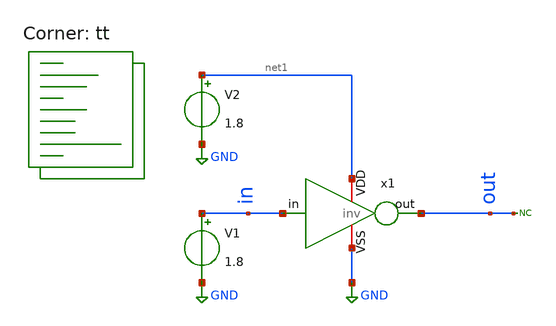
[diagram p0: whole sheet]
** sch_path: xsch/tb/inv/inv_tb.sch
**.subckt inv_tb
x1 in out net1 GND inv
* noconn out
V1 in GND 1.8
V2 net1 GND 1.8
**** begin user architecture code
.lib $::SKYWATER_MODELS/sky130.lib.spice tt



.control
save v(out)
dc V1 0 1.8 0.01
write inv_dc.raw
quit
.endc


**** end user architecture code
**.ends

* expanding   symbol:  ip/inv/inv.sym # of pins=4
** sym_path: xsch/ip/inv/inv.sym
** sch_path: xsch/ip/inv/inv.sch
.subckt inv in out VDD VSS
*.ipin in
*.opin out
*.iopin VDD
*.iopin VSS
XMN out in VSS VSS sky130_fd_pr__nfet_01v8 L=0.15 W=1 nf=1 ad='int((1 + 1)/2) * 1 / 1 * 0.29' as='int((1 + 2)/2) * 1 / 1 * 0.29'
+ pd='2*int((1 + 1)/2) * (1 / 1 + 0.29)' ps='2*int((1 + 2)/2) * (1 / 1 + 0.29)' nrd='0.29 / 1 ' nrs='0.29 / 1 '
+ sa=0 sb=0 sd=0 mult=1 m=1
XMP out in VDD VDD sky130_fd_pr__pfet_01v8 L=0.15 W=2 nf=1 ad='int((nf+1)/2) * W/nf * 0.29' as='int((nf+2)/2) * W/nf * 0.29'
+ pd='2*int((nf+1)/2) * (W/nf + 0.29)' ps='2*int((nf+2)/2) * (W/nf + 0.29)' nrd='0.29 / W' nrs='0.29 / W'
+ sa=0 sb=0 sd=0 mult=1 m=1
.ends

.GLOBAL GND
.end
